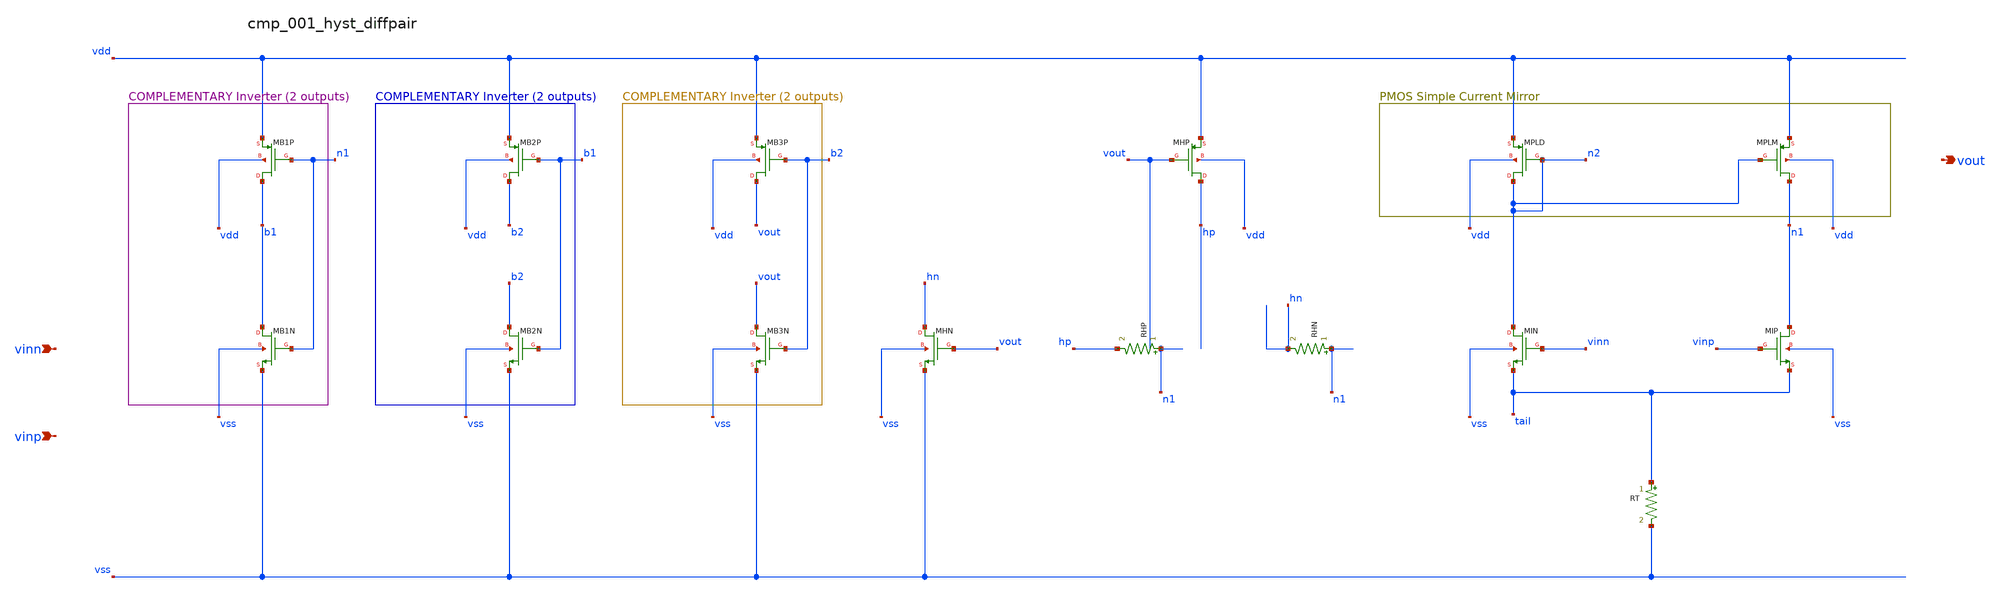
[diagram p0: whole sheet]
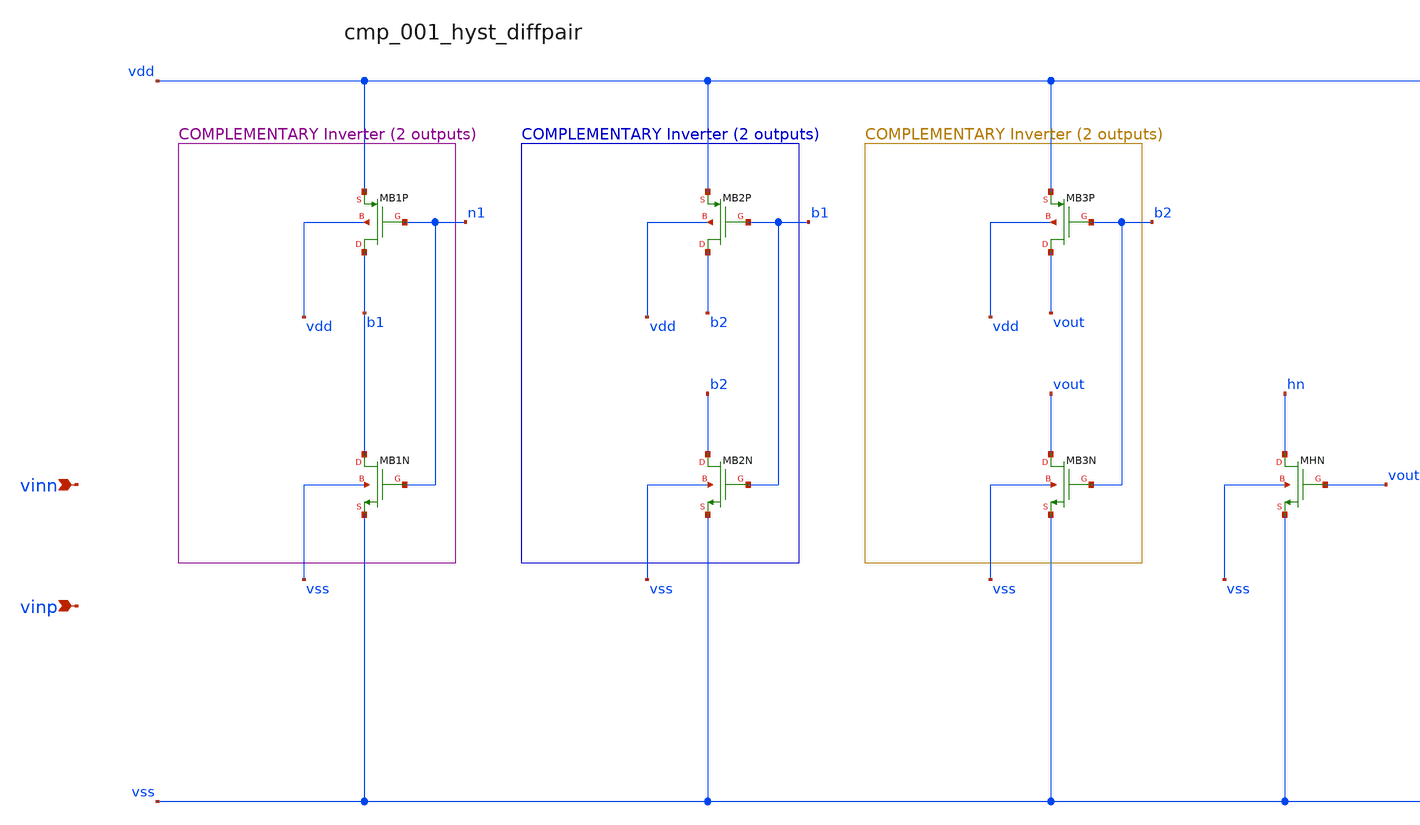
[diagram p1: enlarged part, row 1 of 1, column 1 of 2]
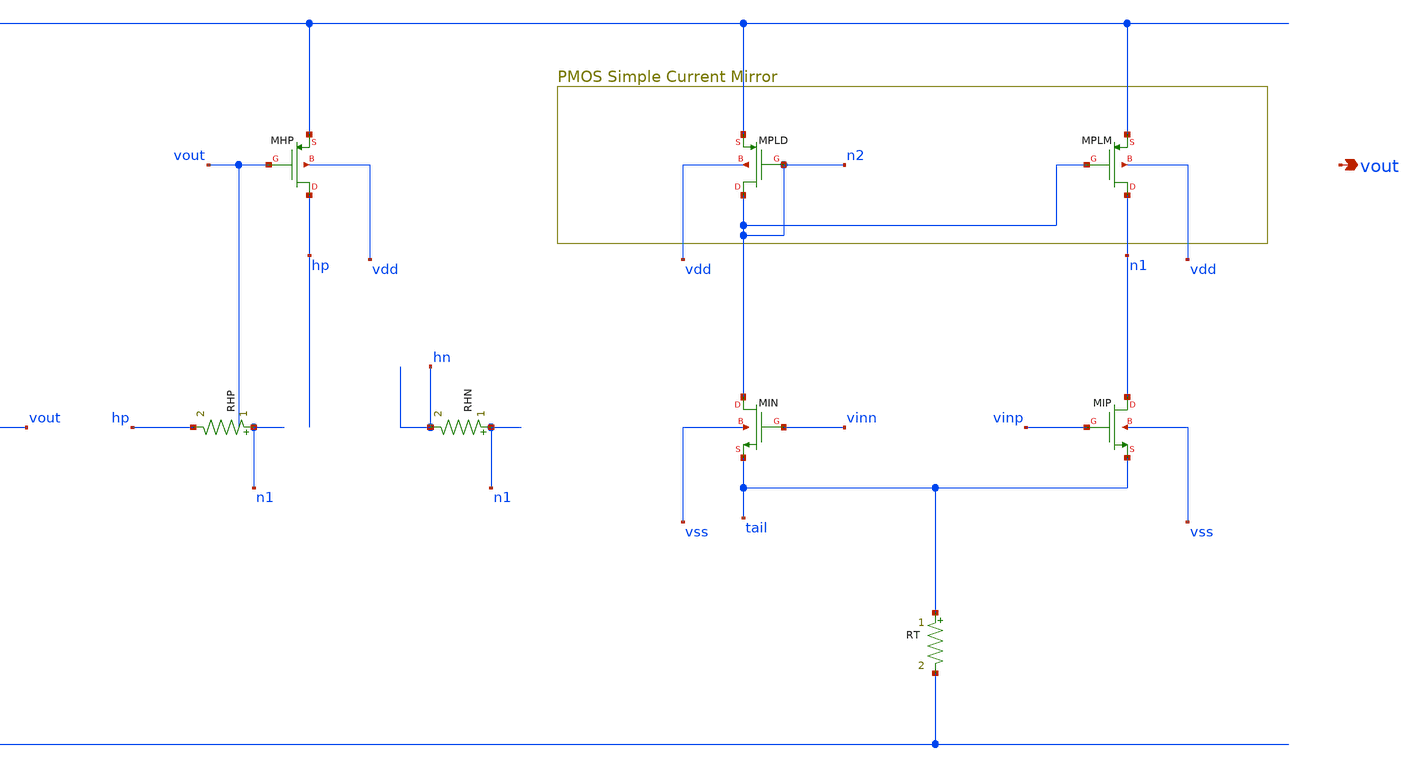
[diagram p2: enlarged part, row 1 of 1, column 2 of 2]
** sch_path: analog-db/raw/cmp_001_hyst_diffpair/cmp_001_hyst_diffpair_annotated.sch
**.subckt cmp_001_hyst_diffpair_annotated vinn vinp vout
*.ipin vinn
*.ipin vinp
*.opin vout
RHN n1 hn x_dut_rhn_value m=1
RHP n1 hp x_dut_rhp_value m=1
RT tail vss x_rtail m=1
XMB1N b1 n1 vss vss sg13_lv_nmos w=x_dut_xmb1n_w l=x_dut_xmb1n_l ng=1 m=x_dut_xmb1n_m
XMB1P b1 n1 vdd vdd sg13_lv_pmos w=x_dut_xmb1p_w l=x_dut_xmb1p_l ng=1 m=x_dut_xmb1p_m
XMB2N b2 b1 vss vss sg13_lv_nmos w=x_dut_xmb2n_w l=x_dut_xmb2n_l ng=1 m=x_dut_xmb2n_m
XMB2P b2 b1 vdd vdd sg13_lv_pmos w=x_dut_xmb2p_w l=x_dut_xmb2p_l ng=1 m=x_dut_xmb2p_m
XMB3N vout b2 vss vss sg13_lv_nmos w=x_dut_xmb3n_w l=x_dut_xmb3n_l ng=1 m=x_dut_xmb3n_m
XMB3P vout b2 vdd vdd sg13_lv_pmos w=x_dut_xmb3p_w l=x_dut_xmb3p_l ng=1 m=x_dut_xmb3p_m
XMHN hn vout vss vss sg13_lv_nmos w=x_dut_xmhn_w l=x_dut_xmhn_l ng=1 m=x_dut_xmhn_m
XMHP hp vout vdd vdd sg13_lv_pmos w=x_dut_xmhp_w l=x_dut_xmhp_l ng=1 m=x_dut_xmhp_m
XMIN n2 vinn tail vss sg13_lv_nmos w=x_dut_xmin_w l=x_dut_xmin_l ng=1 m=x_dut_xmin_m
XMIP n1 vinp tail vss sg13_lv_nmos w=x_dut_xmip_w l=x_dut_xmip_l ng=1 m=x_dut_xmip_m
XMPLD n2 n2 vdd vdd sg13_lv_pmos w=x_dut_xmpld_w l=x_dut_xmpld_l ng=1 m=x_dut_xmpld_m
XMPLM n1 n2 vdd vdd sg13_lv_pmos w=x_dut_xmplm_w l=x_dut_xmplm_l ng=1 m=x_dut_xmplm_m
**.ends
.end
